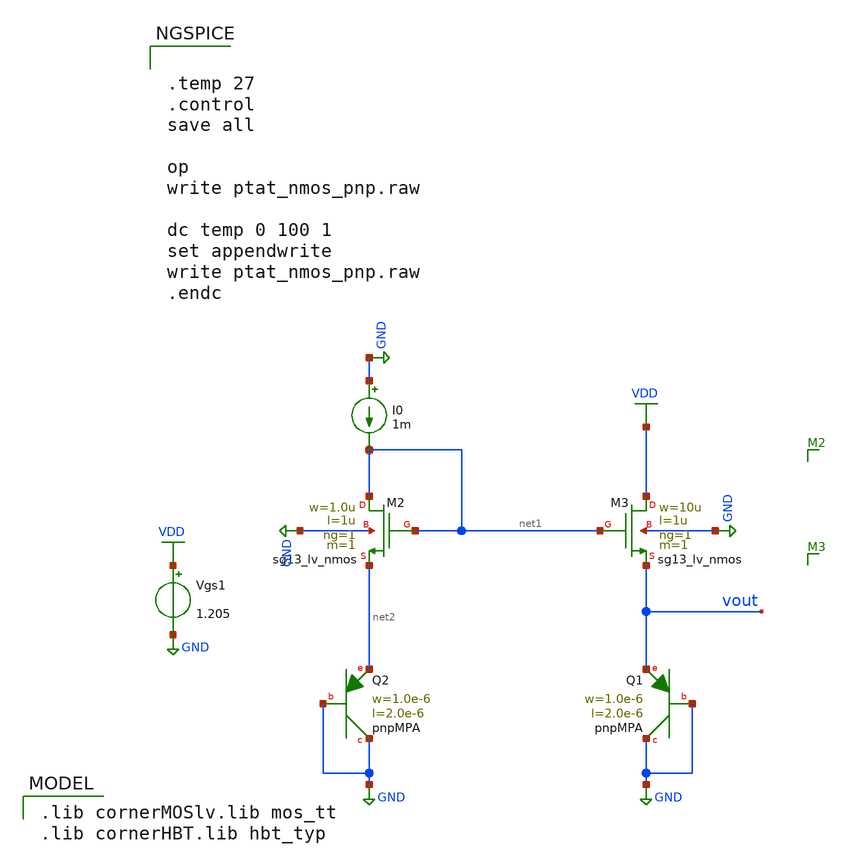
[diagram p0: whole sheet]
** sch_path: xschem/ptat_nmos_with_current_mirror.sch
* Copyright 2023 IHP PDK Authors
**.subckt ptat_nmos_with_current_mirror
XQ1 GND GND vout pnpMPA a=2p p=6u m=1
XQ2 GND GND net2 pnpMPA a=2p p=6u m=1
XM2 net1 net1 net2 GND sg13_lv_nmos w=1.0u l=1u ng=1 m=1 mm_ok=1
XM3 VDD net1 vout GND sg13_lv_nmos w=10u l=1u ng=1 m=1 mm_ok=1
I0 GND net1 1m
Vgs1 VDD GND 1.205
**** begin user architecture code
 .lib cornerMOSlv.lib mos_tt
.lib cornerHBT.lib hbt_typ


.temp 27
.control
save all

op
write ptat_nmos_pnp.raw

dc temp 0 100 1
set appendwrite
write ptat_nmos_pnp.raw
.endc


**** end user architecture code
**.ends
.GLOBAL GND
.GLOBAL VDD
.end
